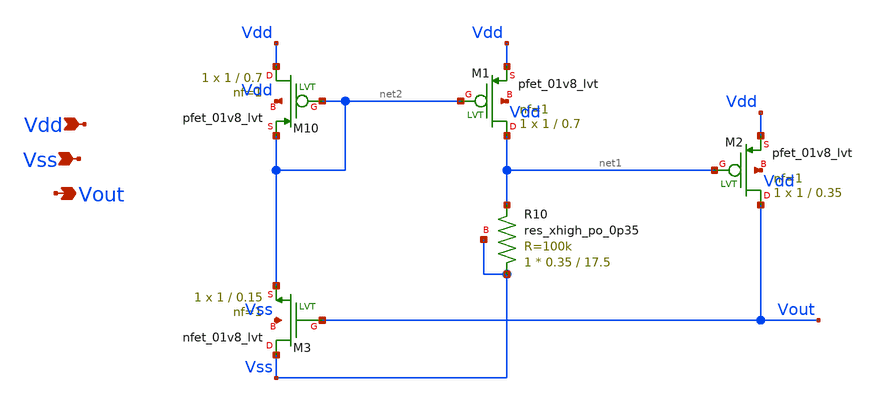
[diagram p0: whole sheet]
** sch_path: tt10-hdl/tt_um_test_commit/xschem/T2/startup/POR/Z_old/resistor-vijh_por.sch
**.subckt resistor-vijh_por Vdd Vss Vout
*.ipin Vdd
*.ipin Vss
*.opin Vout
XM10 Vdd net2 net2 Vdd sky130_fd_pr__pfet_01v8_lvt L=0.7 W=1 nf=1 ad='int((1 + 1)/2) * 1 / 1 * 0.29'
+ as='int((1 + 2)/2) * 1 / 1 * 0.29' pd='2*int((1 + 1)/2) * (1 / 1 + 0.29)' ps='2*int((1 + 2)/2) * (1 / 1 + 0.29)'
+ nrd='0.29 / 1 ' nrs='0.29 / 1 ' sa=0 sb=0 sd=0 mult=1 m=1
XM1 net1 net2 Vdd Vdd sky130_fd_pr__pfet_01v8_lvt L=0.7 W=1 nf=1 ad='int((1 + 1)/2) * 1 / 1 * 0.29' as='int((1 + 2)/2) * 1 / 1 * 0.29'
+ pd='2*int((1 + 1)/2) * (1 / 1 + 0.29)' ps='2*int((1 + 2)/2) * (1 / 1 + 0.29)' nrd='0.29 / 1 ' nrs='0.29 / 1 '
+ sa=0 sb=0 sd=0 mult=1 m=1
XM2 Vout net1 Vdd Vdd sky130_fd_pr__pfet_01v8_lvt L=0.35 W=1 nf=1 ad='int((1 + 1)/2) * 1 / 1 * 0.29'
+ as='int((1 + 2)/2) * 1 / 1 * 0.29' pd='2*int((1 + 1)/2) * (1 / 1 + 0.29)' ps='2*int((1 + 2)/2) * (1 / 1 + 0.29)'
+ nrd='0.29 / 1 ' nrs='0.29 / 1 ' sa=0 sb=0 sd=0 mult=1 m=1
XM3 Vss Vout net2 Vss sky130_fd_pr__nfet_01v8_lvt L=0.15 W=1 nf=1 ad='int((1 + 1)/2) * 1 / 1 * 0.29'
+ as='int((1 + 2)/2) * 1 / 1 * 0.29' pd='2*int((1 + 1)/2) * (1 / 1 + 0.29)' ps='2*int((1 + 2)/2) * (1 / 1 + 0.29)'
+ nrd='0.29 / 1 ' nrs='0.29 / 1 ' sa=0 sb=0 sd=0 mult=1 m=1
XR10 Vss net1 Vss sky130_fd_pr__res_xhigh_po_0p35 L=17.5 mult=1 m=1
**.ends
.end
